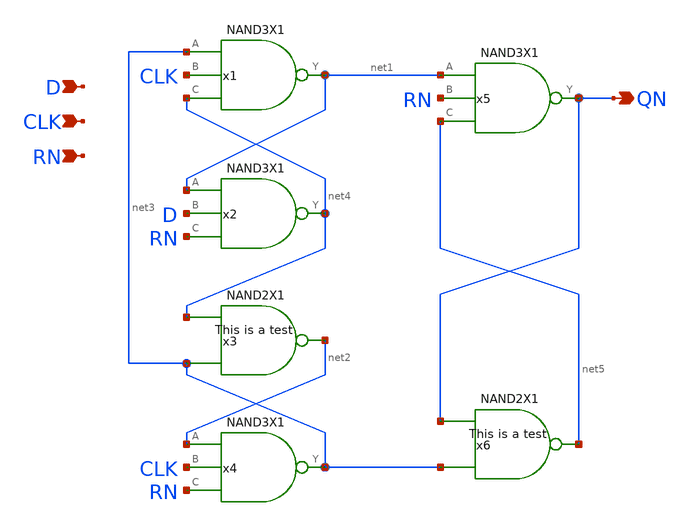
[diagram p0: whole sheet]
** sch_path: lib/xschem/DFFRNQNX1.sch
**.subckt DFFRNQNX1 QN D CLK RN
*.opin QN
*.ipin D
*.ipin CLK
*.ipin RN
x1 net1 net3 CLK net4 VDD VSS NAND3X1
x2 net4 net1 D RN VDD VSS NAND3X1
x3 net2 net4 net3 VDD VSS NAND2X1
x4 net3 net2 CLK RN VDD VSS NAND3X1
x5 QN net1 RN net5 VDD VSS NAND3X1
x6 net5 QN net3 VDD VSS NAND2X1
**.ends
.end
